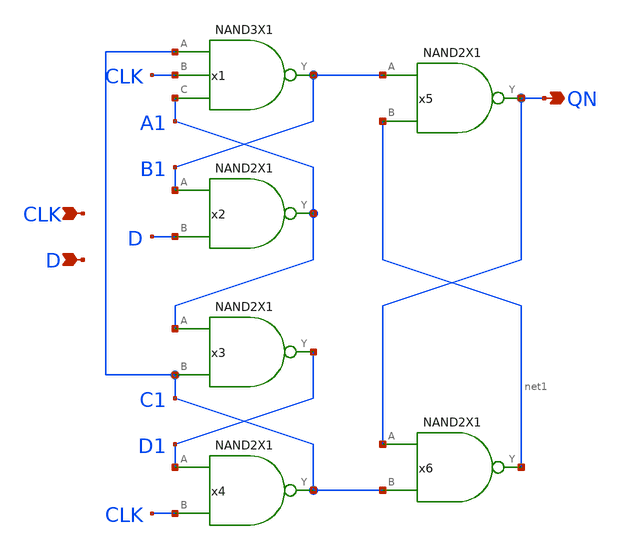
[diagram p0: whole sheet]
** sch_path: lib/xschem/DFFQNX1.sch
**.subckt DFFQNX1 CLK D QN
*.ipin CLK
*.ipin D
*.opin QN
x1 B1 C1 CLK A1 VDD VSS NAND3X1
x2 A1 B1 D VDD VSS NAND2X1
x3 D1 A1 C1 VDD VSS NAND2X1
x4 C1 D1 CLK VDD VSS NAND2X1
x5 QN B1 net1 VDD VSS NAND2X1
x6 net1 QN C1 VDD VSS NAND2X1
**.ends

* expanding   symbol:  NAND3X1.sym # of pins=4
** sym_path: lib/xschem/NAND3X1.sym
** sch_path: lib/xschem/NAND3X1.sch
.subckt NAND3X1 Y A B C VDD VSS
*.ipin A
*.opin Y
*.ipin B
*.ipin C
XM1 net2 C VSS VSS sky130_fd_pr__nfet_01v8 L=0.15 W=3 nf=1 ad='int((nf+1)/2) * W/nf * 0.29' as='int((nf+2)/2) * W/nf * 0.29'
+ pd='2*int((nf+1)/2) * (W/nf + 0.29)' ps='2*int((nf+2)/2) * (W/nf + 0.29)' nrd='0.29 / W' nrs='0.29 / W'
+ sa=0 sb=0 sd=0 mult=1 m=1
XM2 Y A VDD VDD sky130_fd_pr__pfet_01v8 L=0.15 W=2 nf=1 ad='int((nf+1)/2) * W/nf * 0.29' as='int((nf+2)/2) * W/nf * 0.29'
+ pd='2*int((nf+1)/2) * (W/nf + 0.29)' ps='2*int((nf+2)/2) * (W/nf + 0.29)' nrd='0.29 / W' nrs='0.29 / W'
+ sa=0 sb=0 sd=0 mult=1 m=1
XM3 net1 B net2 VSS sky130_fd_pr__nfet_01v8 L=0.15 W=3 nf=1 ad='int((nf+1)/2) * W/nf * 0.29' as='int((nf+2)/2) * W/nf * 0.29'
+ pd='2*int((nf+1)/2) * (W/nf + 0.29)' ps='2*int((nf+2)/2) * (W/nf + 0.29)' nrd='0.29 / W' nrs='0.29 / W'
+ sa=0 sb=0 sd=0 mult=1 m=1
XM4 Y A net1 VSS sky130_fd_pr__nfet_01v8 L=0.15 W=3 nf=1 ad='int((nf+1)/2) * W/nf * 0.29' as='int((nf+2)/2) * W/nf * 0.29'
+ pd='2*int((nf+1)/2) * (W/nf + 0.29)' ps='2*int((nf+2)/2) * (W/nf + 0.29)' nrd='0.29 / W' nrs='0.29 / W'
+ sa=0 sb=0 sd=0 mult=1 m=1
XM5 Y A VDD VDD sky130_fd_pr__pfet_01v8 L=0.15 W=2 nf=1 ad='int((nf+1)/2) * W/nf * 0.29' as='int((nf+2)/2) * W/nf * 0.29'
+ pd='2*int((nf+1)/2) * (W/nf + 0.29)' ps='2*int((nf+2)/2) * (W/nf + 0.29)' nrd='0.29 / W' nrs='0.29 / W'
+ sa=0 sb=0 sd=0 mult=1 m=1
XM6 Y B VDD VDD sky130_fd_pr__pfet_01v8 L=0.15 W=2 nf=1 ad='int((nf+1)/2) * W/nf * 0.29' as='int((nf+2)/2) * W/nf * 0.29'
+ pd='2*int((nf+1)/2) * (W/nf + 0.29)' ps='2*int((nf+2)/2) * (W/nf + 0.29)' nrd='0.29 / W' nrs='0.29 / W'
+ sa=0 sb=0 sd=0 mult=1 m=1
XM7 Y B VDD VDD sky130_fd_pr__pfet_01v8 L=0.15 W=2 nf=1 ad='int((nf+1)/2) * W/nf * 0.29' as='int((nf+2)/2) * W/nf * 0.29'
+ pd='2*int((nf+1)/2) * (W/nf + 0.29)' ps='2*int((nf+2)/2) * (W/nf + 0.29)' nrd='0.29 / W' nrs='0.29 / W'
+ sa=0 sb=0 sd=0 mult=1 m=1
XM8 Y C VDD VDD sky130_fd_pr__pfet_01v8 L=0.15 W=2 nf=1 ad='int((nf+1)/2) * W/nf * 0.29' as='int((nf+2)/2) * W/nf * 0.29'
+ pd='2*int((nf+1)/2) * (W/nf + 0.29)' ps='2*int((nf+2)/2) * (W/nf + 0.29)' nrd='0.29 / W' nrs='0.29 / W'
+ sa=0 sb=0 sd=0 mult=1 m=1
XM9 Y C VDD VDD sky130_fd_pr__pfet_01v8 L=0.15 W=2 nf=1 ad='int((nf+1)/2) * W/nf * 0.29' as='int((nf+2)/2) * W/nf * 0.29'
+ pd='2*int((nf+1)/2) * (W/nf + 0.29)' ps='2*int((nf+2)/2) * (W/nf + 0.29)' nrd='0.29 / W' nrs='0.29 / W'
+ sa=0 sb=0 sd=0 mult=1 m=1
.ends


* expanding   symbol:  NAND2X1.sym # of pins=3
** sym_path: lib/xschem/NAND2X1.sym
** sch_path: lib/xschem/NAND2X1.sch
.subckt NAND2X1 Y A B VDD VSS
*.ipin A
*.opin Y
*.ipin B
XM1 Y A VDD VDD sky130_fd_pr__pfet_01v8 L=0.15 W=2 nf=1 ad='int((nf+1)/2) * W/nf * 0.29' as='int((nf+2)/2) * W/nf * 0.29'
+ pd='2*int((nf+1)/2) * (W/nf + 0.29)' ps='2*int((nf+2)/2) * (W/nf + 0.29)' nrd='0.29 / W' nrs='0.29 / W'
+ sa=0 sb=0 sd=0 mult=1 m=1
XM5 Y A net1 VSS sky130_fd_pr__nfet_01v8 L=0.15 W=3 nf=1 ad='int((nf+1)/2) * W/nf * 0.29' as='int((nf+2)/2) * W/nf * 0.29'
+ pd='2*int((nf+1)/2) * (W/nf + 0.29)' ps='2*int((nf+2)/2) * (W/nf + 0.29)' nrd='0.29 / W' nrs='0.29 / W'
+ sa=0 sb=0 sd=0 mult=1 m=1
XM2 Y A VDD VDD sky130_fd_pr__pfet_01v8 L=0.15 W=2 nf=1 ad='int((nf+1)/2) * W/nf * 0.29' as='int((nf+2)/2) * W/nf * 0.29'
+ pd='2*int((nf+1)/2) * (W/nf + 0.29)' ps='2*int((nf+2)/2) * (W/nf + 0.29)' nrd='0.29 / W' nrs='0.29 / W'
+ sa=0 sb=0 sd=0 mult=1 m=1
XM3 Y B VDD VDD sky130_fd_pr__pfet_01v8 L=0.15 W=2 nf=1 ad='int((nf+1)/2) * W/nf * 0.29' as='int((nf+2)/2) * W/nf * 0.29'
+ pd='2*int((nf+1)/2) * (W/nf + 0.29)' ps='2*int((nf+2)/2) * (W/nf + 0.29)' nrd='0.29 / W' nrs='0.29 / W'
+ sa=0 sb=0 sd=0 mult=1 m=1
XM4 Y B VDD VDD sky130_fd_pr__pfet_01v8 L=0.15 W=2 nf=1 ad='int((nf+1)/2) * W/nf * 0.29' as='int((nf+2)/2) * W/nf * 0.29'
+ pd='2*int((nf+1)/2) * (W/nf + 0.29)' ps='2*int((nf+2)/2) * (W/nf + 0.29)' nrd='0.29 / W' nrs='0.29 / W'
+ sa=0 sb=0 sd=0 mult=1 m=1
XM6 net1 B VSS VSS sky130_fd_pr__nfet_01v8 L=0.15 W=3 nf=1 ad='int((nf+1)/2) * W/nf * 0.29' as='int((nf+2)/2) * W/nf * 0.29'
+ pd='2*int((nf+1)/2) * (W/nf + 0.29)' ps='2*int((nf+2)/2) * (W/nf + 0.29)' nrd='0.29 / W' nrs='0.29 / W'
+ sa=0 sb=0 sd=0 mult=1 m=1
.ends

.end
